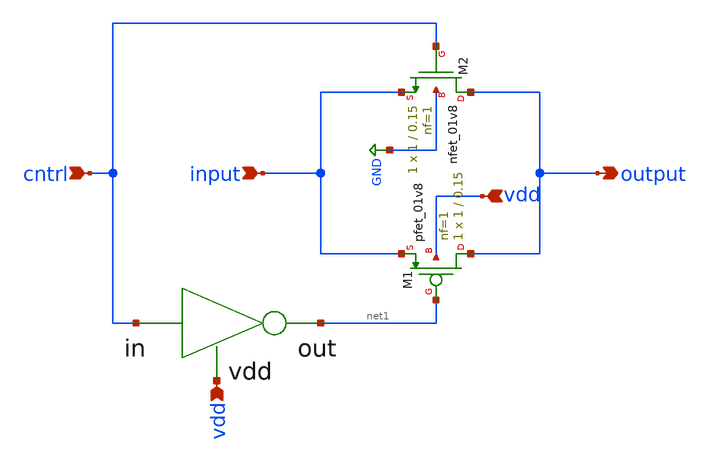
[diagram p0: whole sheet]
** sch_path: xschem/attenuator/trans-gate.sch
**.subckt trans-gate vdd vdd input cntrl output
*.ipin vdd
*.ipin vdd
*.ipin input
*.ipin cntrl
*.opin output
XM1 output net1 input vdd sky130_fd_pr__pfet_01v8 L=0.15 W=1 nf=1 ad='int((nf+1)/2) * W/nf * 0.29' as='int((nf+2)/2) * W/nf * 0.29'
+ pd='2*int((nf+1)/2) * (W/nf + 0.29)' ps='2*int((nf+2)/2) * (W/nf + 0.29)' nrd='0.29 / W' nrs='0.29 / W'
+ sa=0 sb=0 sd=0 mult=1 m=1
XM2 output cntrl input GND sky130_fd_pr__nfet_01v8 L=0.15 W=1 nf=1 ad='int((nf+1)/2) * W/nf * 0.29' as='int((nf+2)/2) * W/nf * 0.29'
+ pd='2*int((nf+1)/2) * (W/nf + 0.29)' ps='2*int((nf+2)/2) * (W/nf + 0.29)' nrd='0.29 / W' nrs='0.29 / W'
+ sa=0 sb=0 sd=0 mult=1 m=1
**** begin user architecture code
 ** manual skywater pdks install (with patches applied)
* .lib $::SKYWATER_MODELS/models/sky130.lib.spice tt

** opencircuitdesign pdks install
.lib $::SKYWATER_MODELS/sky130.lib.spice tt

.param mc_mm_switch=0
.param mc_pr_switch=0

**** end user architecture code
**.ends
.GLOBAL GND
.end
